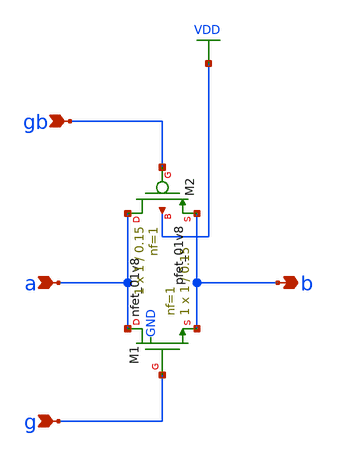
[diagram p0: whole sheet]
** sch_path: trans_gate.sch
**.subckt trans_gate gb a g b
*.ipin gb
*.ipin a
*.ipin g
*.opin b
XM1 a g b GND sky130_fd_pr__nfet_01v8 L=0.15 W=1 nf=1 ad='int((nf+1)/2) * W/nf * 0.29' as='int((nf+2)/2) * W/nf * 0.29'
+ pd='2*int((nf+1)/2) * (W/nf + 0.29)' ps='2*int((nf+2)/2) * (W/nf + 0.29)' nrd='0.29 / W' nrs='0.29 / W'
+ sa=0 sb=0 sd=0 mult=1 m=1
XM2 a gb b VDD sky130_fd_pr__pfet_01v8 L=0.15 W=1 nf=1 ad='int((nf+1)/2) * W/nf * 0.29' as='int((nf+2)/2) * W/nf * 0.29'
+ pd='2*int((nf+1)/2) * (W/nf + 0.29)' ps='2*int((nf+2)/2) * (W/nf + 0.29)' nrd='0.29 / W' nrs='0.29 / W'
+ sa=0 sb=0 sd=0 mult=1 m=1
**.ends
.GLOBAL VDD
.end
